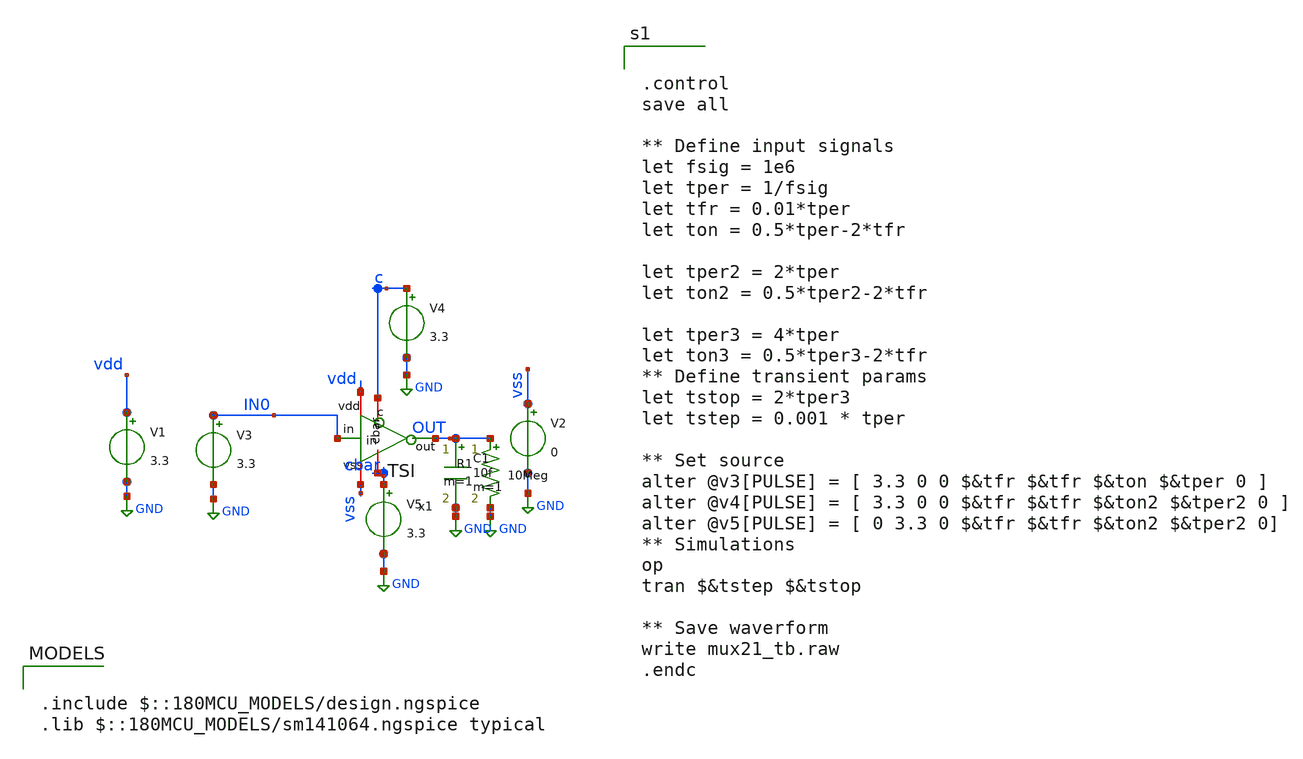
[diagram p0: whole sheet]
** sch_path: schematics/PC/TSI/TSI_tb.sch
**.subckt TSI_tb
V2 vss GND 0
V1 vdd GND 3.3
V3 IN0 GND 3.3
V5 cbar GND 3.3
C1 OUT GND 10f m=1
x1 vdd c OUT IN0 cbar vss TSI
V4 c GND 3.3
R1 OUT GND 10Meg m=1
**** begin user architecture code

.include $::180MCU_MODELS/design.ngspice
.lib $::180MCU_MODELS/sm141064.ngspice typical



.control
save all

** Define input signals
let fsig = 1e6
let tper = 1/fsig
let tfr = 0.01*tper
let ton = 0.5*tper-2*tfr

let tper2 = 2*tper
let ton2 = 0.5*tper2-2*tfr

let tper3 = 4*tper
let ton3 = 0.5*tper3-2*tfr
** Define transient params
let tstop = 2*tper3
let tstep = 0.001 * tper

** Set source
alter @v3[PULSE] = [ 3.3 0 0 $&tfr $&tfr $&ton $&tper 0 ]
alter @v4[PULSE] = [ 3.3 0 0 $&tfr $&tfr $&ton2 $&tper2 0 ]
alter @v5[PULSE] = [ 0 3.3 0 $&tfr $&tfr $&ton2 $&tper2 0]
** Simulations
op
tran $&tstep $&tstop

** Save waverform
write mux21_tb.raw
.endc



**** end user architecture code
**.ends

* expanding   symbol:  CAD2/TSI.sym # of pins=6
** sym_path: schematics/PC/TSI/TSI.sym
** sch_path: schematics/PC/TSI/TSI.sch
.subckt TSI vdd c out in cbar vss
*.ipin in
*.opin out
*.iopin vdd
*.iopin vss
*.iopin cbar
*.iopin c
XM1 net1 c vdd vdd pfet_03v3 L=0.28u W=4u nf=1 ad='int((nf+1)/2) * W/nf * 0.18u' as='int((nf+2)/2) * W/nf * 0.18u'
+ pd='2*int((nf+1)/2) * (W/nf + 0.18u)' ps='2*int((nf+2)/2) * (W/nf + 0.18u)' nrd='0.18u / W' nrs='0.18u / W'
+ sa=0 sb=0 sd=0 m=1
XM2 out in net1 vdd pfet_03v3 L=0.28u W=4u nf=1 ad='int((nf+1)/2) * W/nf * 0.18u' as='int((nf+2)/2) * W/nf * 0.18u'
+ pd='2*int((nf+1)/2) * (W/nf + 0.18u)' ps='2*int((nf+2)/2) * (W/nf + 0.18u)' nrd='0.18u / W' nrs='0.18u / W'
+ sa=0 sb=0 sd=0 m=1
XM3 out in net2 vss nfet_03v3 L=0.28u W=2u nf=1 ad='int((nf+1)/2) * W/nf * 0.18u' as='int((nf+2)/2) * W/nf * 0.18u'
+ pd='2*int((nf+1)/2) * (W/nf + 0.18u)' ps='2*int((nf+2)/2) * (W/nf + 0.18u)' nrd='0.18u / W' nrs='0.18u / W'
+ sa=0 sb=0 sd=0 m=1
XM4 net2 cbar vss vss nfet_03v3 L=0.28u W=2u nf=1 ad='int((nf+1)/2) * W/nf * 0.18u' as='int((nf+2)/2) * W/nf * 0.18u'
+ pd='2*int((nf+1)/2) * (W/nf + 0.18u)' ps='2*int((nf+2)/2) * (W/nf + 0.18u)' nrd='0.18u / W' nrs='0.18u / W'
+ sa=0 sb=0 sd=0 m=1
.ends

.GLOBAL GND
.end
